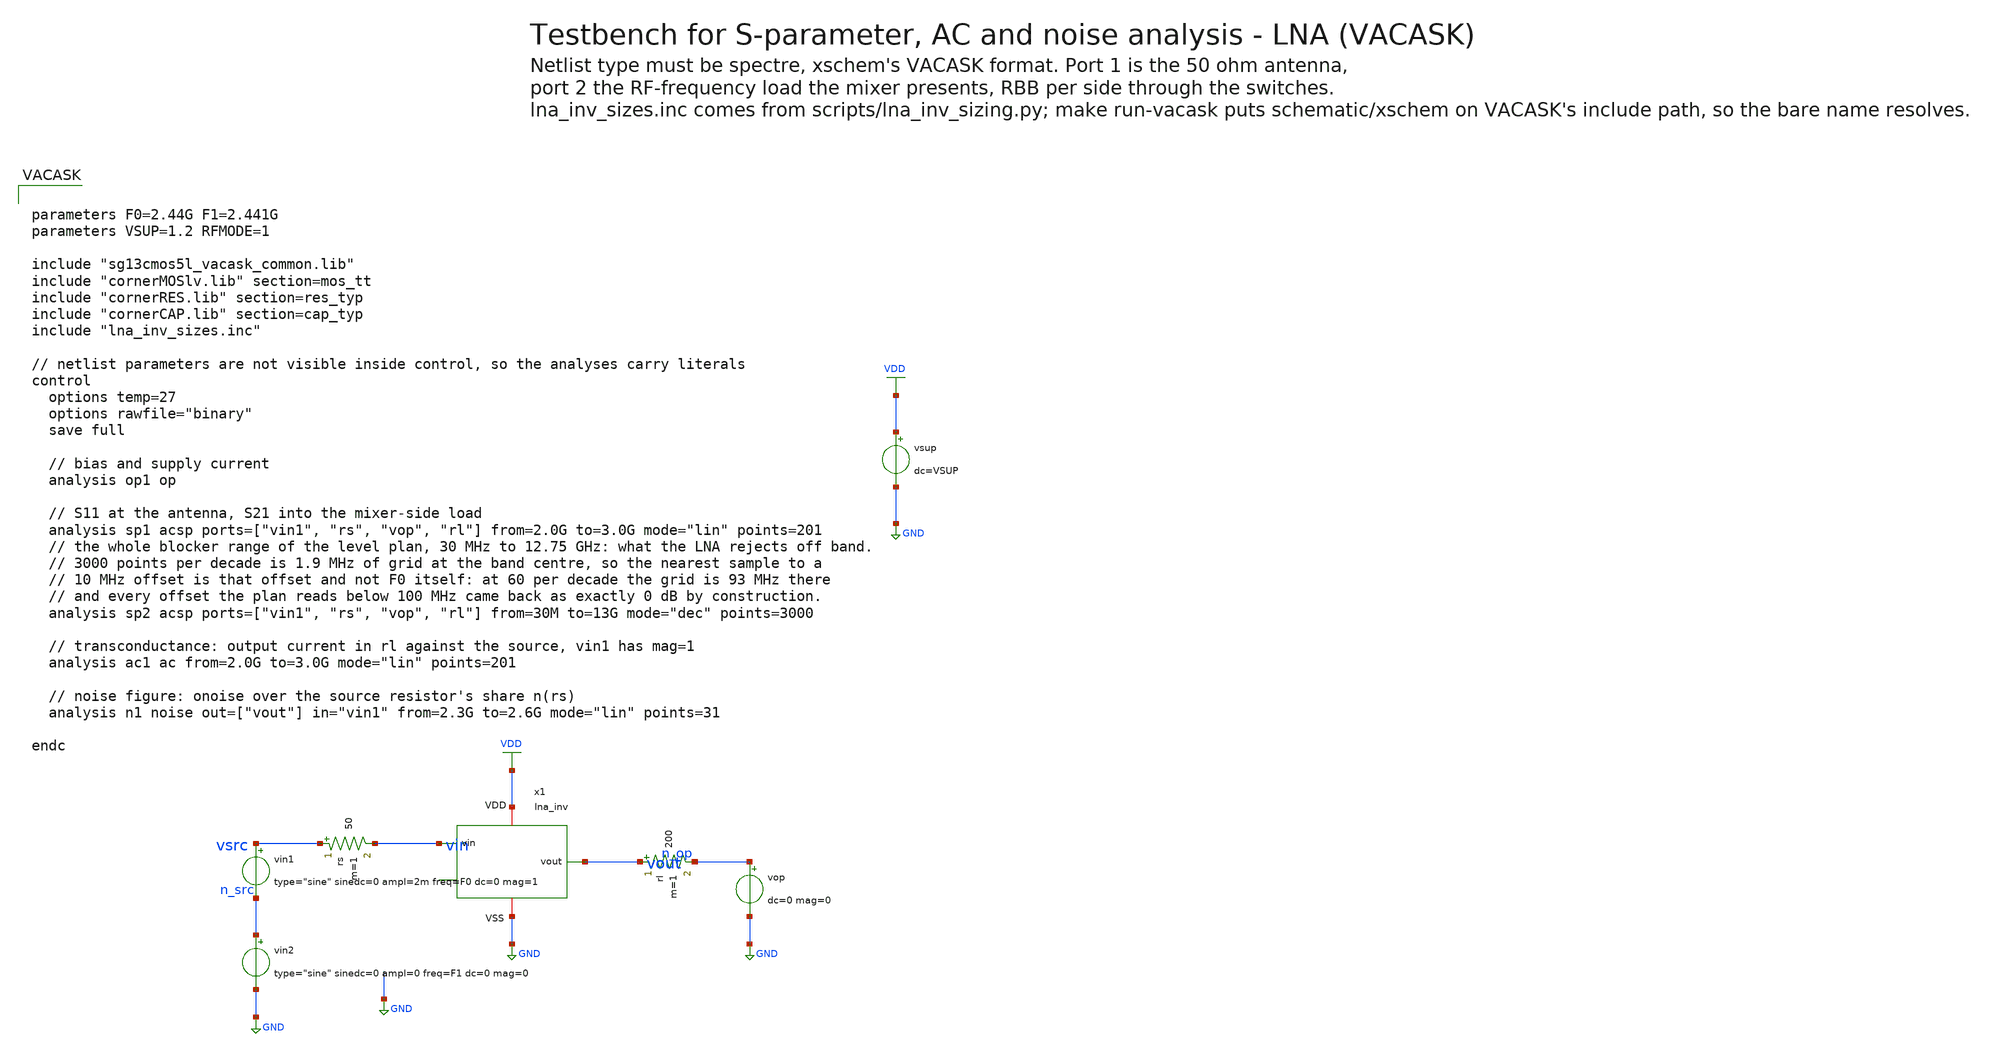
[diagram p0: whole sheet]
** sch_path: macros/lna_inv/testbenches/xschem/lna_inv_tb_sp.sch
**.subckt lna_inv_tb_sp
vin1 vsrc n_src type="sine" sinedc=0 ampl=2m freq=F0 dc=0 mag=1
vin2 n_src GND type="sine" sinedc=0 ampl=0 freq=F1 dc=0 mag=0
rs vsrc vin 50 m=1
x1 vin vout VDD GND lna_inv
rl vout n_op 200 m=1
vop n_op GND dc=0 mag=0
vsup VDD GND dc=VSUP
**** begin user architecture code


parameters F0=2.44G F1=2.441G
parameters VSUP=1.2 RFMODE=1

include "sg13cmos5l_vacask_common.lib"
include "cornerMOSlv.lib" section=mos_tt
include "cornerRES.lib" section=res_typ
include "cornerCAP.lib" section=cap_typ
include "lna_inv_sizes.inc"

// netlist parameters are not visible inside control, so the analyses carry literals
control
  options temp=27
  options rawfile="binary"
  save full

  // bias and supply current
  analysis op1 op

  // S11 at the antenna, S21 into the mixer-side load
  analysis sp1 acsp ports=["vin1", "rs", "vop", "rl"] from=2.0G to=3.0G mode="lin" points=201
  // the whole blocker range of the level plan, 30 MHz to 12.75 GHz: what the LNA rejects off band.
  // 3000 points per decade is 1.9 MHz of grid at the band centre, so the nearest sample to a
  // 10 MHz offset is that offset and not F0 itself: at 60 per decade the grid is 93 MHz there
  // and every offset the plan reads below 100 MHz came back as exactly 0 dB by construction.
  analysis sp2 acsp ports=["vin1", "rs", "vop", "rl"] from=30M to=13G mode="dec" points=3000

  // transconductance: output current in rl against the source, vin1 has mag=1
  analysis ac1 ac from=2.0G to=3.0G mode="lin" points=201

  // noise figure: onoise over the source resistor's share n(rs)
  analysis n1 noise out=["vout"] in="vin1" from=2.3G to=2.6G mode="lin" points=31

endc


**** end user architecture code
**.ends
.GLOBAL GND
.GLOBAL VDD
.end
